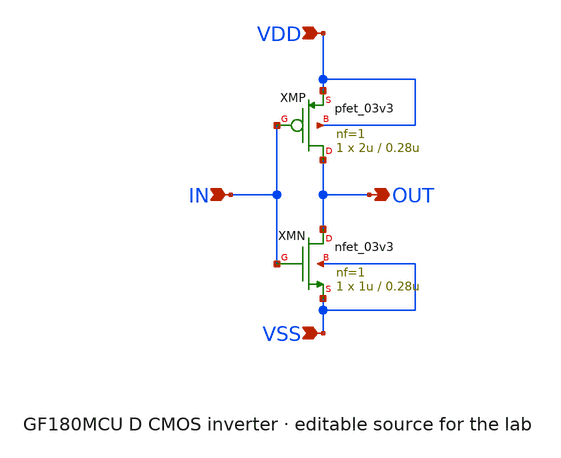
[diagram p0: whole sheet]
** sch_path: examples/gf180_inverter/inverter.sch
**.subckt inverter IN OUT VDD VSS
*.ipin IN
*.opin OUT
*.ipin VDD
*.ipin VSS
XMN OUT IN VSS VSS nfet_03v3 L=0.28u W=1u nf=1 ad=0.44p as=0.44p pd=2.88u ps=2.88u nrd=0 nrs=0 sa=0
+ sb=0 sd=0 m=1
XMP OUT IN VDD VDD pfet_03v3 L=0.28u W=2u nf=1 ad=0.88p as=0.88p pd=4.88u ps=4.88u nrd=0 nrs=0 sa=0
+ sb=0 sd=0 m=1
**.ends
.end
